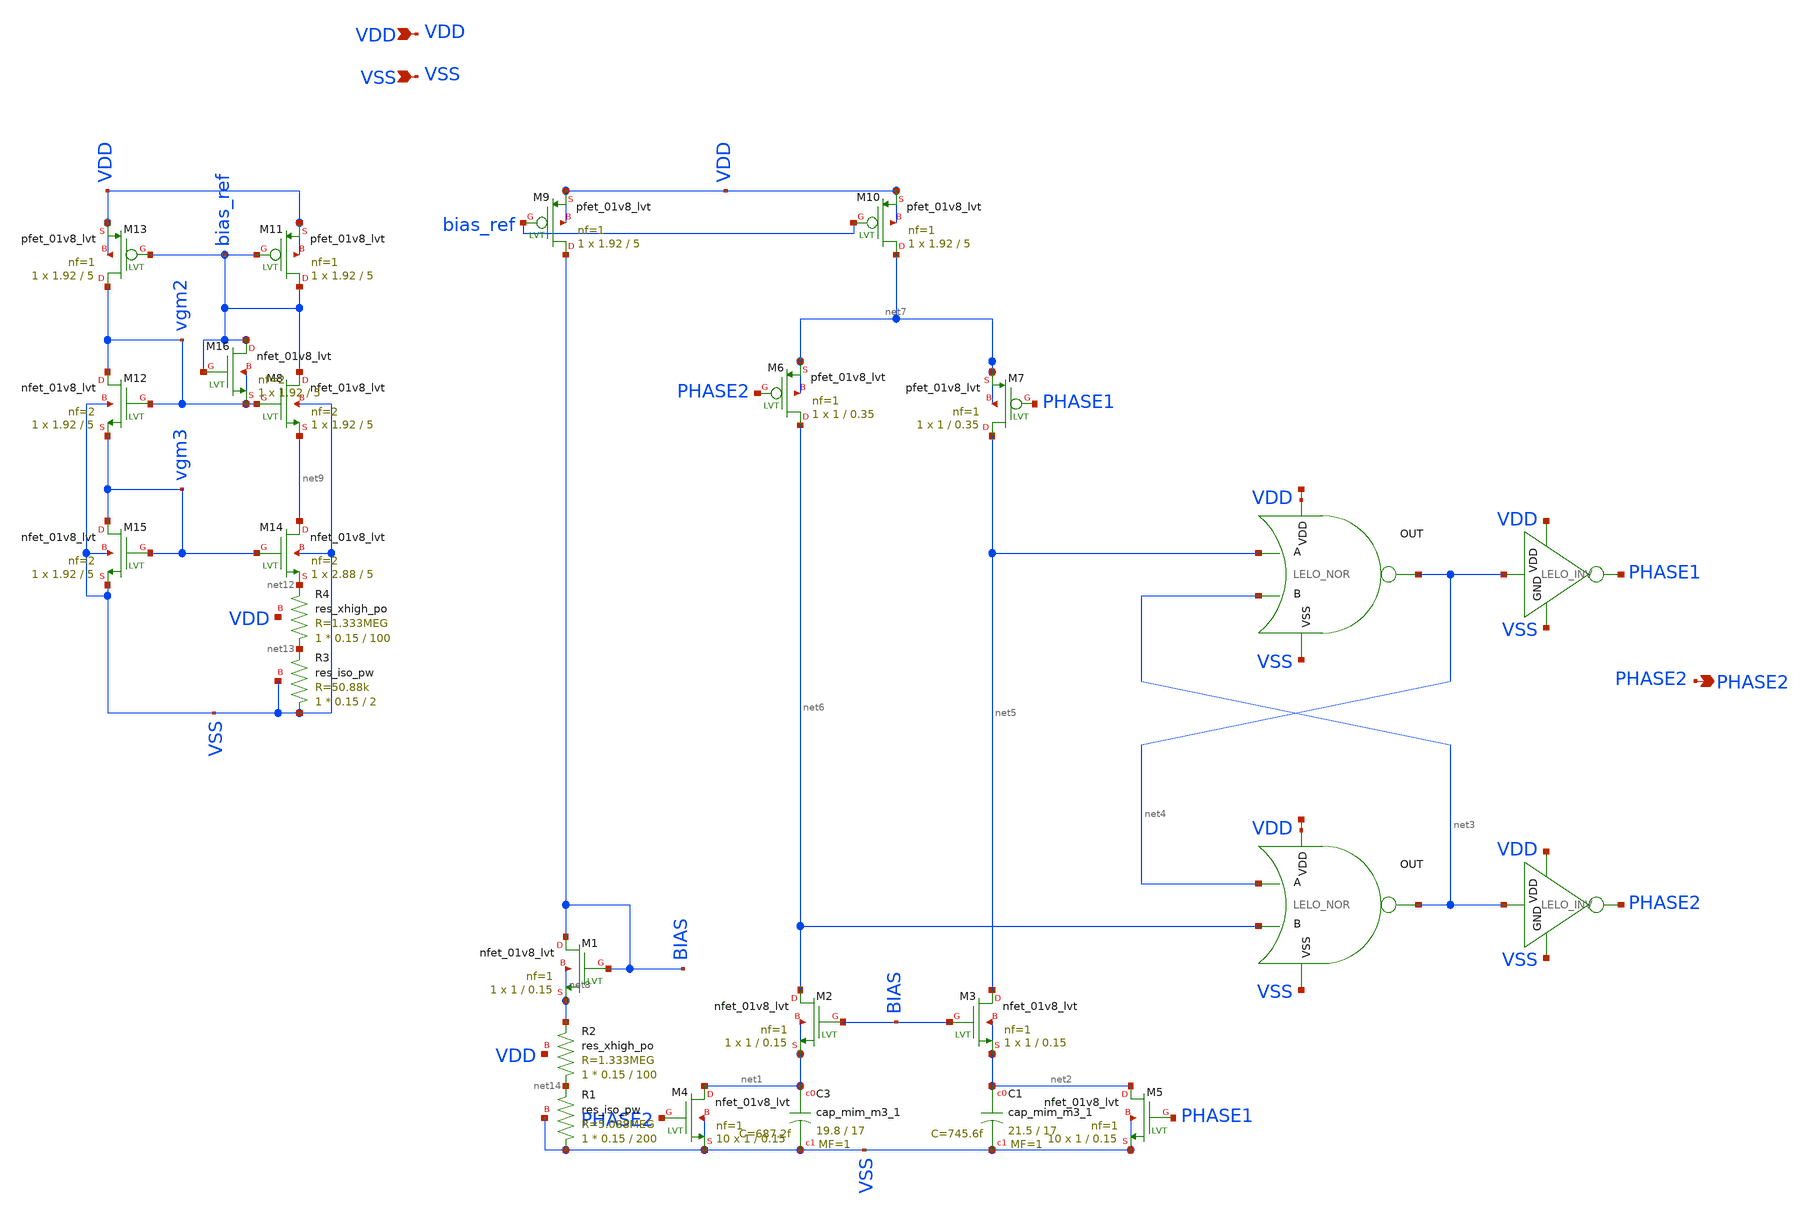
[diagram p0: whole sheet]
** sch_path: design/LELO_SVOD_SKY130A/LELO_SVOD_RELOSC.sch
**.subckt LELO_SVOD_RELOSC VDD VSS PHASE2
*.ipin VDD
*.ipin VSS
*.opin PHASE2
XM1 BIAS BIAS net8 net8 sky130_fd_pr__nfet_01v8_lvt L=0.15 W=1 nf=1 ad='int((1 + 1)/2) * 1 / 1 * 0.29'
+ as='int((1 + 2)/2) * 1 / 1 * 0.29' pd='2*int((1 + 1)/2) * (1 / 1 + 0.29)' ps='2*int((1 + 2)/2) * (1 / 1 + 0.29)'
+ nrd='0.29 / 1 ' nrs='0.29 / 1 ' sa=0 sb=0 sd=0 mult=1 m=1
XM2 net6 BIAS net1 net1 sky130_fd_pr__nfet_01v8_lvt L=0.15 W=1 nf=1 ad='int((1 + 1)/2) * 1 / 1 * 0.29'
+ as='int((1 + 2)/2) * 1 / 1 * 0.29' pd='2*int((1 + 1)/2) * (1 / 1 + 0.29)' ps='2*int((1 + 2)/2) * (1 / 1 + 0.29)'
+ nrd='0.29 / 1 ' nrs='0.29 / 1 ' sa=0 sb=0 sd=0 mult=1 m=1
XM3 net5 BIAS net2 net2 sky130_fd_pr__nfet_01v8_lvt L=0.15 W=1 nf=1 ad='int((1 + 1)/2) * 1 / 1 * 0.29'
+ as='int((1 + 2)/2) * 1 / 1 * 0.29' pd='2*int((1 + 1)/2) * (1 / 1 + 0.29)' ps='2*int((1 + 2)/2) * (1 / 1 + 0.29)'
+ nrd='0.29 / 1 ' nrs='0.29 / 1 ' sa=0 sb=0 sd=0 mult=1 m=1
XM4 net1 PHASE2 VSS VSS sky130_fd_pr__nfet_01v8_lvt L=0.15 W=1 nf=1 ad='int((1 + 1)/2) * 1 / 1 * 0.29'
+ as='int((1 + 2)/2) * 1 / 1 * 0.29' pd='2*int((1 + 1)/2) * (1 / 1 + 0.29)' ps='2*int((1 + 2)/2) * (1 / 1 + 0.29)'
+ nrd='0.29 / 1 ' nrs='0.29 / 1 ' sa=0 sb=0 sd=0 mult=10 m=10
XM5 net2 PHASE1 VSS VSS sky130_fd_pr__nfet_01v8_lvt L=0.15 W=1 nf=1 ad='int((1 + 1)/2) * 1 / 1 * 0.29'
+ as='int((1 + 2)/2) * 1 / 1 * 0.29' pd='2*int((1 + 1)/2) * (1 / 1 + 0.29)' ps='2*int((1 + 2)/2) * (1 / 1 + 0.29)'
+ nrd='0.29 / 1 ' nrs='0.29 / 1 ' sa=0 sb=0 sd=0 mult=10 m=10
x1 net10 net4 net5 net3 VSS LELO_NOR
x2 net11 net3 net4 net6 VSS LELO_NOR
XM6 net6 PHASE2 net7 net7 sky130_fd_pr__pfet_01v8_lvt L=0.35 W=1 nf=1 ad='int((1 + 1)/2) * 1 / 1 * 0.29'
+ as='int((1 + 2)/2) * 1 / 1 * 0.29' pd='2*int((1 + 1)/2) * (1 / 1 + 0.29)' ps='2*int((1 + 2)/2) * (1 / 1 + 0.29)'
+ nrd='0.29 / 1 ' nrs='0.29 / 1 ' sa=0 sb=0 sd=0 mult=1 m=1
XM7 net5 PHASE1 net7 net7 sky130_fd_pr__pfet_01v8_lvt L=0.35 W=1 nf=1 ad='int((1 + 1)/2) * 1 / 1 * 0.29'
+ as='int((1 + 2)/2) * 1 / 1 * 0.29' pd='2*int((1 + 1)/2) * (1 / 1 + 0.29)' ps='2*int((1 + 2)/2) * (1 / 1 + 0.29)'
+ nrd='0.29 / 1 ' nrs='0.29 / 1 ' sa=0 sb=0 sd=0 mult=1 m=1
x3 VDD net4 PHASE1 VSS LELO_INV
x4 VDD net3 PHASE2 VSS LELO_INV
XM9 BIAS bias_ref VDD VDD sky130_fd_pr__pfet_01v8_lvt L=5 W=1.92 nf=1 ad='int((1 + 1)/2) * 1.92 / 1 * 0.29'
+ as='int((1 + 2)/2) * 1.92 / 1 * 0.29' pd='2*int((1 + 1)/2) * (1.92 / 1 + 0.29)' ps='2*int((1 + 2)/2) * (1.92 / 1 + 0.29)'
+ nrd='0.29 / 1.92 ' nrs='0.29 / 1.92 ' sa=0 sb=0 sd=0 mult=1 m=1
XM10 net7 bias_ref VDD VDD sky130_fd_pr__pfet_01v8_lvt L=5 W=1.92 nf=1 ad='int((1 + 1)/2) * 1.92 / 1 * 0.29'
+ as='int((1 + 2)/2) * 1.92 / 1 * 0.29' pd='2*int((1 + 1)/2) * (1.92 / 1 + 0.29)' ps='2*int((1 + 2)/2) * (1.92 / 1 + 0.29)'
+ nrd='0.29 / 1.92 ' nrs='0.29 / 1.92 ' sa=0 sb=0 sd=0 mult=1 m=1
XM8 bias_ref vgm2 net9 VSS sky130_fd_pr__nfet_01v8_lvt L=5 W=1.92 nf=2 ad='int((2 + 1)/2) * 1.92 / 2 * 0.29'
+ as='int((2 + 2)/2) * 1.92 / 2 * 0.29' pd='2*int((2 + 1)/2) * (1.92 / 2 + 0.29)' ps='2*int((2 + 2)/2) * (1.92 / 2 + 0.29)'
+ nrd='0.29 / 1.92 ' nrs='0.29 / 1.92 ' sa=0 sb=0 sd=0 mult=1 m=1
XM11 bias_ref bias_ref VDD VDD sky130_fd_pr__pfet_01v8_lvt L=5 W=1.92 nf=1 ad='int((1 + 1)/2) * 1.92 / 1 * 0.29'
+ as='int((1 + 2)/2) * 1.92 / 1 * 0.29' pd='2*int((1 + 1)/2) * (1.92 / 1 + 0.29)' ps='2*int((1 + 2)/2) * (1.92 / 1 + 0.29)'
+ nrd='0.29 / 1.92 ' nrs='0.29 / 1.92 ' sa=0 sb=0 sd=0 mult=1 m=1
XM12 vgm2 vgm2 vgm3 VSS sky130_fd_pr__nfet_01v8_lvt L=5 W=1.92 nf=2 ad='int((2 + 1)/2) * 1.92 / 2 * 0.29'
+ as='int((2 + 2)/2) * 1.92 / 2 * 0.29' pd='2*int((2 + 1)/2) * (1.92 / 2 + 0.29)' ps='2*int((2 + 2)/2) * (1.92 / 2 + 0.29)'
+ nrd='0.29 / 1.92 ' nrs='0.29 / 1.92 ' sa=0 sb=0 sd=0 mult=1 m=1
XM13 vgm2 bias_ref VDD VDD sky130_fd_pr__pfet_01v8_lvt L=5 W=1.92 nf=1 ad='int((1 + 1)/2) * 1.92 / 1 * 0.29'
+ as='int((1 + 2)/2) * 1.92 / 1 * 0.29' pd='2*int((1 + 1)/2) * (1.92 / 1 + 0.29)' ps='2*int((1 + 2)/2) * (1.92 / 1 + 0.29)'
+ nrd='0.29 / 1.92 ' nrs='0.29 / 1.92 ' sa=0 sb=0 sd=0 mult=1 m=1
XM14 net9 vgm3 net12 VSS sky130_fd_pr__nfet_01v8_lvt L=5 W=2.88 nf=2 ad='int((2 + 1)/2) * 2.88 / 2 * 0.29'
+ as='int((2 + 2)/2) * 2.88 / 2 * 0.29' pd='2*int((2 + 1)/2) * (2.88 / 2 + 0.29)' ps='2*int((2 + 2)/2) * (2.88 / 2 + 0.29)'
+ nrd='0.29 / 2.88 ' nrs='0.29 / 2.88 ' sa=0 sb=0 sd=0 mult=1 m=1
XM15 vgm3 vgm3 VSS VSS sky130_fd_pr__nfet_01v8_lvt L=5 W=1.92 nf=2 ad='int((2 + 1)/2) * 1.92 / 2 * 0.29'
+ as='int((2 + 2)/2) * 1.92 / 2 * 0.29' pd='2*int((2 + 1)/2) * (1.92 / 2 + 0.29)' ps='2*int((2 + 2)/2) * (1.92 / 2 + 0.29)'
+ nrd='0.29 / 1.92 ' nrs='0.29 / 1.92 ' sa=0 sb=0 sd=0 mult=1 m=1
XM16 bias_ref bias_ref vgm2 vgm2 sky130_fd_pr__nfet_01v8_lvt L=5 W=1.92 nf=2 ad='int((2 + 1)/2) * 1.92 / 2 * 0.29'
+ as='int((2 + 2)/2) * 1.92 / 2 * 0.29' pd='2*int((2 + 1)/2) * (1.92 / 2 + 0.29)' ps='2*int((2 + 2)/2) * (1.92 / 2 + 0.29)'
+ nrd='0.29 / 1.92 ' nrs='0.29 / 1.92 ' sa=0 sb=0 sd=0 mult=1 m=1
XC3 net1 VSS sky130_fd_pr__cap_mim_m3_1 W=19.8 L=17 MF=1 m=1
XC1 net2 VSS sky130_fd_pr__cap_mim_m3_1 W=21.5 L=17 MF=1 m=1
XR3 VSS net13 VSS sky130_fd_pr__res_iso_pw W=0.15 L=2 m=1
XR1 VSS net14 VSS sky130_fd_pr__res_iso_pw W=0.15 L=200 m=1
XR4 net13 net12 VDD sky130_fd_pr__res_xhigh_po W=0.15 L=100 mult=1 m=1
XR2 net14 net8 VDD sky130_fd_pr__res_xhigh_po W=0.15 L=100 mult=1 m=1
**.ends

* expanding   symbol:  LELO_SVOD_SKY130A/LELO_NOR.sym # of pins=5
** sym_path: design/LELO_SVOD_SKY130A/LELO_NOR.sym
** sch_path: design/LELO_SVOD_SKY130A/LELO_NOR.sch
.subckt LELO_NOR VDD OUT A B VSS
*.ipin VDD
*.ipin VSS
*.opin OUT
*.ipin A
*.ipin B
XM2 OUT B VSS VSS sky130_fd_pr__nfet_01v8 L=0.15 W=2 nf=1 ad='int((1 + 1)/2) * 2 / 1 * 0.29' as='int((1 + 2)/2) * 2 / 1 * 0.29'
+ pd='2*int((1 + 1)/2) * (2 / 1 + 0.29)' ps='2*int((1 + 2)/2) * (2 / 1 + 0.29)' nrd='0.29 / 2 ' nrs='0.29 / 2 '
+ sa=0 sb=0 sd=0 mult=1 m=1
XM1 OUT A VSS VSS sky130_fd_pr__nfet_01v8 L=0.15 W=2 nf=1 ad='int((1 + 1)/2) * 2 / 1 * 0.29' as='int((1 + 2)/2) * 2 / 1 * 0.29'
+ pd='2*int((1 + 1)/2) * (2 / 1 + 0.29)' ps='2*int((1 + 2)/2) * (2 / 1 + 0.29)' nrd='0.29 / 2 ' nrs='0.29 / 2 '
+ sa=0 sb=0 sd=0 mult=1 m=1
XM3 OUT B net1 VDD sky130_fd_pr__pfet_01v8 L=0.15 W=4 nf=1 ad='int((1 + 1)/2) * 4 / 1 * 0.29' as='int((1 + 2)/2) * 4 / 1 * 0.29'
+ pd='2*int((1 + 1)/2) * (4 / 1 + 0.29)' ps='2*int((1 + 2)/2) * (4 / 1 + 0.29)' nrd='0.29 / 4 ' nrs='0.29 / 4 '
+ sa=0 sb=0 sd=0 mult=1 m=1
XM4 net1 A VDD VDD sky130_fd_pr__pfet_01v8 L=0.15 W=4 nf=1 ad='int((1 + 1)/2) * 4 / 1 * 0.29' as='int((1 + 2)/2) * 4 / 1 * 0.29'
+ pd='2*int((1 + 1)/2) * (4 / 1 + 0.29)' ps='2*int((1 + 2)/2) * (4 / 1 + 0.29)' nrd='0.29 / 4 ' nrs='0.29 / 4 '
+ sa=0 sb=0 sd=0 mult=1 m=1
.ends


* expanding   symbol:  LELO_SVOD_SKY130A/LELO_INV.sym # of pins=4
** sym_path: design/LELO_SVOD_SKY130A/LELO_INV.sym
** sch_path: design/LELO_SVOD_SKY130A/LELO_INV.sch
.subckt LELO_INV VDD VIN VOUT GND
*.ipin VIN
*.ipin VDD
*.ipin GND
*.opin VOUT
XM1 VOUT VIN GND GND sky130_fd_pr__nfet_01v8_lvt L=0.15 W=1 nf=1 ad='int((1 + 1)/2) * 1 / 1 * 0.29' as='int((1 + 2)/2) * 1 / 1 * 0.29'
+ pd='2*int((1 + 1)/2) * (1 / 1 + 0.29)' ps='2*int((1 + 2)/2) * (1 / 1 + 0.29)' nrd='0.29 / 1 ' nrs='0.29 / 1 '
+ sa=0 sb=0 sd=0 mult=1 m=1
XM2 VOUT VIN VDD VDD sky130_fd_pr__pfet_01v8_lvt L=0.35 W=1 nf=1 ad='int((1 + 1)/2) * 1 / 1 * 0.29' as='int((1 + 2)/2) * 1 / 1 * 0.29'
+ pd='2*int((1 + 1)/2) * (1 / 1 + 0.29)' ps='2*int((1 + 2)/2) * (1 / 1 + 0.29)' nrd='0.29 / 1 ' nrs='0.29 / 1 '
+ sa=0 sb=0 sd=0 mult=2 m=2
.ends

.end
